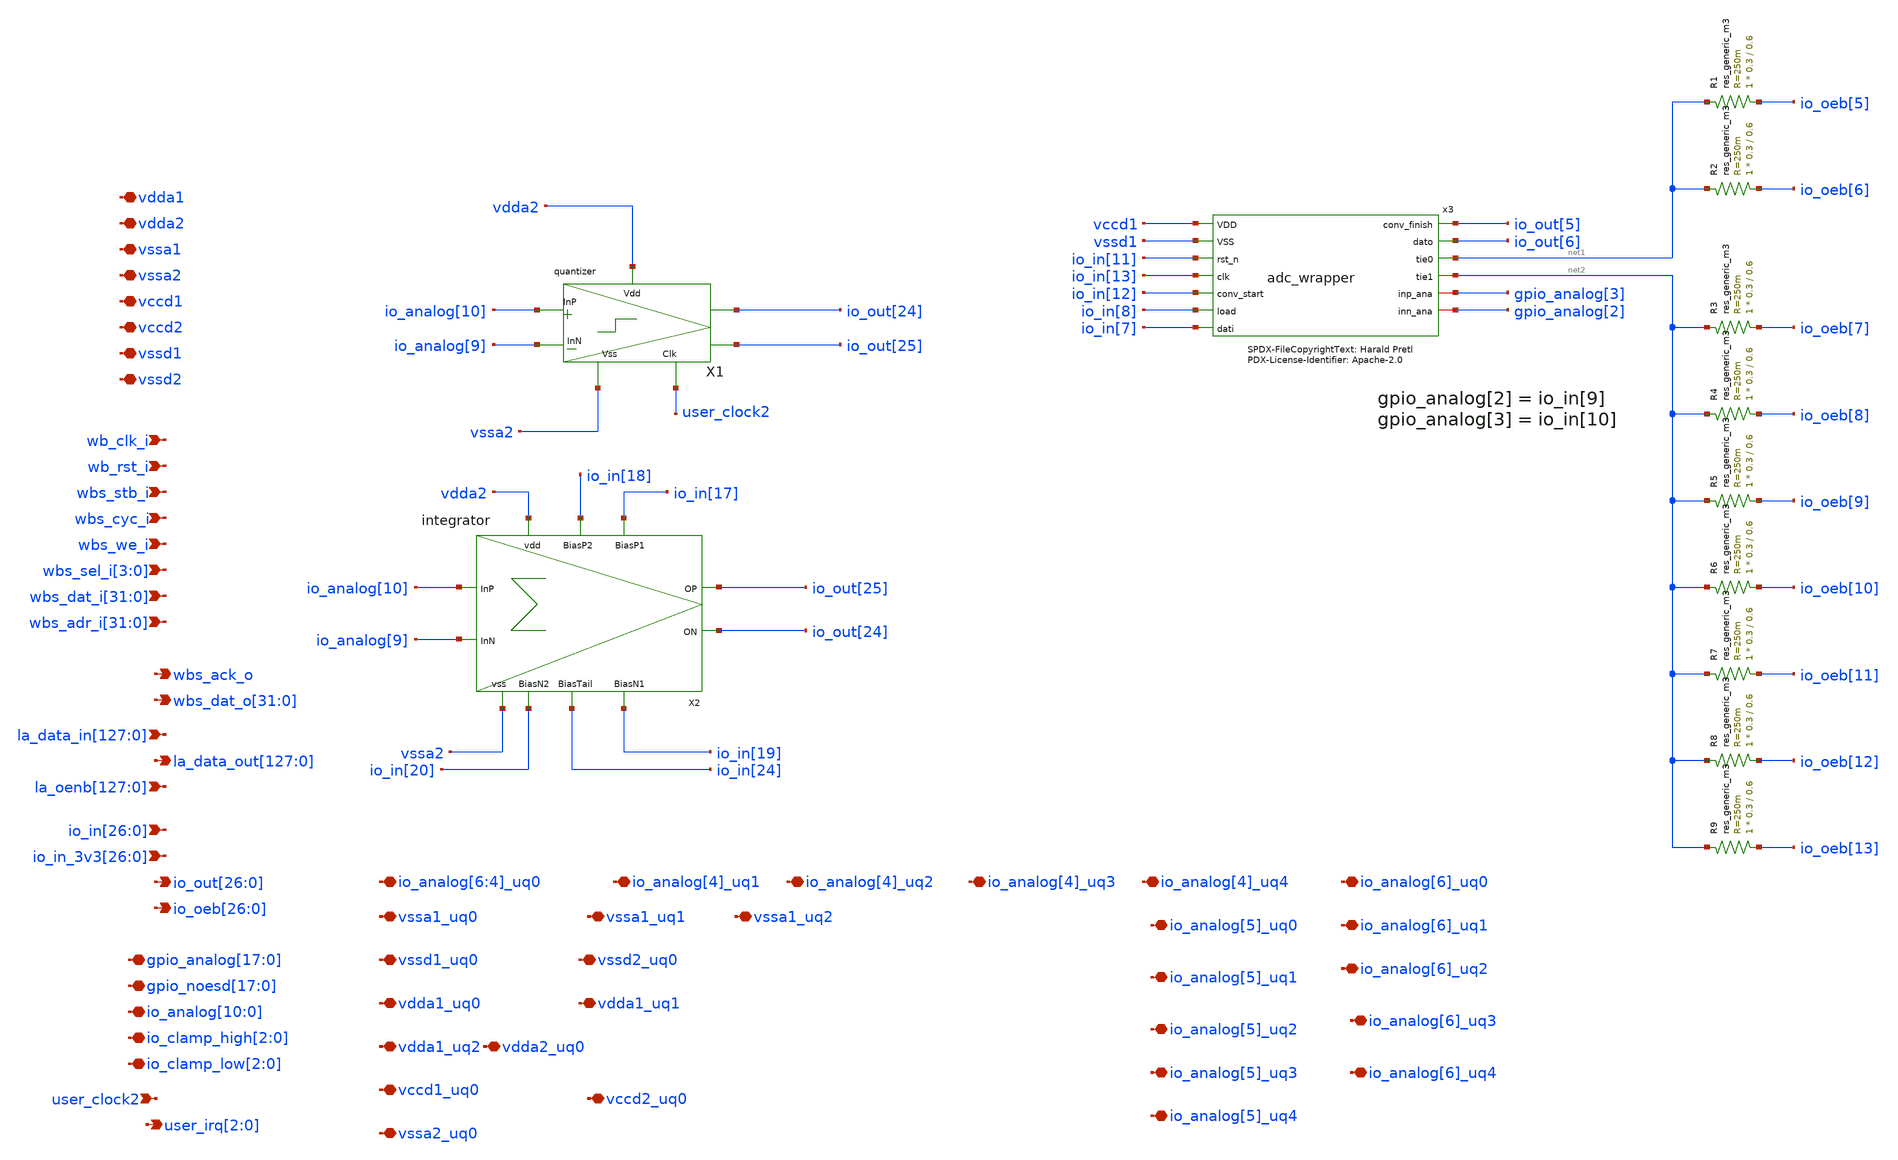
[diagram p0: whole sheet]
** sch_path: xschem/user_analog_project_wrapper_empty.sch
**.subckt user_analog_project_wrapper_empty vdda1 vdda2 vssa1 vssa2 vccd1 vccd2 vssd1 vssd2 wb_clk_i
*+ wb_rst_i wbs_stb_i wbs_cyc_i wbs_we_i wbs_sel_i[3],wbs_sel_i[2],wbs_sel_i[1],wbs_sel_i[0]
*+ wbs_dat_i[31],wbs_dat_i[30],wbs_dat_i[29],wbs_dat_i[28],wbs_dat_i[27],wbs_dat_i[26],wbs_dat_i[25],wbs_dat_i[24],wbs_dat_i[23],wbs_dat_i[22],wbs_dat_i[21],wbs_dat_i[20],wbs_dat_i[19],wbs_dat_i[18],wbs_dat_i[17],wbs_dat_i[16],wbs_dat_i[15],wbs_dat_i[14],wbs_dat_i[13],wbs_dat_i[12],wbs_dat_i[11],wbs_dat_i[10],wbs_dat_i[9],wbs_dat_i[8],wbs_dat_i[7],wbs_dat_i[6],wbs_dat_i[5],wbs_dat_i[4],wbs_dat_i[3],wbs_dat_i[2],wbs_dat_i[1],wbs_dat_i[0]
*+ wbs_adr_i[31],wbs_adr_i[30],wbs_adr_i[29],wbs_adr_i[28],wbs_adr_i[27],wbs_adr_i[26],wbs_adr_i[25],wbs_adr_i[24],wbs_adr_i[23],wbs_adr_i[22],wbs_adr_i[21],wbs_adr_i[20],wbs_adr_i[19],wbs_adr_i[18],wbs_adr_i[17],wbs_adr_i[16],wbs_adr_i[15],wbs_adr_i[14],wbs_adr_i[13],wbs_adr_i[12],wbs_adr_i[11],wbs_adr_i[10],wbs_adr_i[9],wbs_adr_i[8],wbs_adr_i[7],wbs_adr_i[6],wbs_adr_i[5],wbs_adr_i[4],wbs_adr_i[3],wbs_adr_i[2],wbs_adr_i[1],wbs_adr_i[0] wbs_ack_o
*+ wbs_dat_o[31],wbs_dat_o[30],wbs_dat_o[29],wbs_dat_o[28],wbs_dat_o[27],wbs_dat_o[26],wbs_dat_o[25],wbs_dat_o[24],wbs_dat_o[23],wbs_dat_o[22],wbs_dat_o[21],wbs_dat_o[20],wbs_dat_o[19],wbs_dat_o[18],wbs_dat_o[17],wbs_dat_o[16],wbs_dat_o[15],wbs_dat_o[14],wbs_dat_o[13],wbs_dat_o[12],wbs_dat_o[11],wbs_dat_o[10],wbs_dat_o[9],wbs_dat_o[8],wbs_dat_o[7],wbs_dat_o[6],wbs_dat_o[5],wbs_dat_o[4],wbs_dat_o[3],wbs_dat_o[2],wbs_dat_o[1],wbs_dat_o[0]
*+ la_data_in[127],la_data_in[126],la_data_in[125],la_data_in[124],la_data_in[123],la_data_in[122],la_data_in[121],la_data_in[120],la_data_in[119],la_data_in[118],la_data_in[117],la_data_in[116],la_data_in[115],la_data_in[114],la_data_in[113],la_data_in[112],la_data_in[111],la_data_in[110],la_data_in[109],la_data_in[108],la_data_in[107],la_data_in[106],la_data_in[105],la_data_in[104],la_data_in[103],la_data_in[102],la_data_in[101],la_data_in[100],la_data_in[99],la_data_in[98],la_data_in[97],la_data_in[96],la_data_in[95],la_data_in[94],la_data_in[93],la_data_in[92],la_data_in[91],la_data_in[90],la_data_in[89],la_data_in[88],la_data_in[87],la_data_in[86],la_data_in[85],la_data_in[84],la_data_in[83],la_data_in[82],la_data_in[81],la_data_in[80],la_data_in[79],la_data_in[78],la_data_in[77],la_data_in[76],la_data_in[75],la_data_in[74],la_data_in[73],la_data_in[72],la_data_in[71],la_data_in[70],la_data_in[69],la_data_in[68],la_data_in[67],la_data_in[66],la_data_in[65],la_data_in[64],la_data_in[63],la_data_in[62],la_data_in[61],la_data_in[60],la_data_in[59],la_data_in[58],la_data_in[57],la_data_in[56],la_data_in[55],la_data_in[54],la_data_in[53],la_data_in[52],la_data_in[51],la_data_in[50],la_data_in[49],la_data_in[48],la_data_in[47],la_data_in[46],la_data_in[45],la_data_in[44],la_data_in[43],la_data_in[42],la_data_in[41],la_data_in[40],la_data_in[39],la_data_in[38],la_data_in[37],la_data_in[36],la_data_in[35],la_data_in[34],la_data_in[33],la_data_in[32],la_data_in[31],la_data_in[30],la_data_in[29],la_data_in[28],la_data_in[27],la_data_in[26],la_data_in[25],la_data_in[24],la_data_in[23],la_data_in[22],la_data_in[21],la_data_in[20],la_data_in[19],la_data_in[18],la_data_in[17],la_data_in[16],la_data_in[15],la_data_in[14],la_data_in[13],la_data_in[12],la_data_in[11],la_data_in[10],la_data_in[9],la_data_in[8],la_data_in[7],la_data_in[6],la_data_in[5],la_data_in[4],la_data_in[3],la_data_in[2],la_data_in[1],la_data_in[0]
*+ la_data_out[127],la_data_out[126],la_data_out[125],la_data_out[124],la_data_out[123],la_data_out[122],la_data_out[121],la_data_out[120],la_data_out[119],la_data_out[118],la_data_out[117],la_data_out[116],la_data_out[115],la_data_out[114],la_data_out[113],la_data_out[112],la_data_out[111],la_data_out[110],la_data_out[109],la_data_out[108],la_data_out[107],la_data_out[106],la_data_out[105],la_data_out[104],la_data_out[103],la_data_out[102],la_data_out[101],la_data_out[100],la_data_out[99],la_data_out[98],la_data_out[97],la_data_out[96],la_data_out[95],la_data_out[94],la_data_out[93],la_data_out[92],la_data_out[91],la_data_out[90],la_data_out[89],la_data_out[88],la_data_out[87],la_data_out[86],la_data_out[85],la_data_out[84],la_data_out[83],la_data_out[82],la_data_out[81],la_data_out[80],la_data_out[79],la_data_out[78],la_data_out[77],la_data_out[76],la_data_out[75],la_data_out[74],la_data_out[73],la_data_out[72],la_data_out[71],la_data_out[70],la_data_out[69],la_data_out[68],la_data_out[67],la_data_out[66],la_data_out[65],la_data_out[64],la_data_out[63],la_data_out[62],la_data_out[61],la_data_out[60],la_data_out[59],la_data_out[58],la_data_out[57],la_data_out[56],la_data_out[55],la_data_out[54],la_data_out[53],la_data_out[52],la_data_out[51],la_data_out[50],la_data_out[49],la_data_out[48],la_data_out[47],la_data_out[46],la_data_out[45],la_data_out[44],la_data_out[43],la_data_out[42],la_data_out[41],la_data_out[40],la_data_out[39],la_data_out[38],la_data_out[37],la_data_out[36],la_data_out[35],la_data_out[34],la_data_out[33],la_data_out[32],la_data_out[31],la_data_out[30],la_data_out[29],la_data_out[28],la_data_out[27],la_data_out[26],la_data_out[25],la_data_out[24],la_data_out[23],la_data_out[22],la_data_out[21],la_data_out[20],la_data_out[19],la_data_out[18],la_data_out[17],la_data_out[16],la_data_out[15],la_data_out[14],la_data_out[13],la_data_out[12],la_data_out[11],la_data_out[10],la_data_out[9],la_data_out[8],la_data_out[7],la_data_out[6],la_data_out[5],la_data_out[4],la_data_out[3],la_data_out[2],la_data_out[1],la_data_out[0]
*+ io_in[26],io_in[25],io_in[24],io_in[23],io_in[22],io_in[21],io_in[20],io_in[19],io_in[18],io_in[17],io_in[16],io_in[15],io_in[14],io_in[13],io_in[12],io_in[11],io_in[10],io_in[9],io_in[8],io_in[7],io_in[6],io_in[5],io_in[4],io_in[3],io_in[2],io_in[1],io_in[0]
*+ io_in_3v3[26],io_in_3v3[25],io_in_3v3[24],io_in_3v3[23],io_in_3v3[22],io_in_3v3[21],io_in_3v3[20],io_in_3v3[19],io_in_3v3[18],io_in_3v3[17],io_in_3v3[16],io_in_3v3[15],io_in_3v3[14],io_in_3v3[13],io_in_3v3[12],io_in_3v3[11],io_in_3v3[10],io_in_3v3[9],io_in_3v3[8],io_in_3v3[7],io_in_3v3[6],io_in_3v3[5],io_in_3v3[4],io_in_3v3[3],io_in_3v3[2],io_in_3v3[1],io_in_3v3[0] user_clock2
*+ io_out[26],io_out[25],io_out[24],io_out[23],io_out[22],io_out[21],io_out[20],io_out[19],io_out[18],io_out[17],io_out[16],io_out[15],io_out[14],io_out[13],io_out[12],io_out[11],io_out[10],io_out[9],io_out[8],io_out[7],io_out[6],io_out[5],io_out[4],io_out[3],io_out[2],io_out[1],io_out[0]
*+ io_oeb[26],io_oeb[25],io_oeb[24],io_oeb[23],io_oeb[22],io_oeb[21],io_oeb[20],io_oeb[19],io_oeb[18],io_oeb[17],io_oeb[16],io_oeb[15],io_oeb[14],io_oeb[13],io_oeb[12],io_oeb[11],io_oeb[10],io_oeb[9],io_oeb[8],io_oeb[7],io_oeb[6],io_oeb[5],io_oeb[4],io_oeb[3],io_oeb[2],io_oeb[1],io_oeb[0]
*+ gpio_analog[17],gpio_analog[16],gpio_analog[15],gpio_analog[14],gpio_analog[13],gpio_analog[12],gpio_analog[11],gpio_analog[10],gpio_analog[9],gpio_analog[8],gpio_analog[7],gpio_analog[6],gpio_analog[5],gpio_analog[4],gpio_analog[3],gpio_analog[2],gpio_analog[1],gpio_analog[0]
*+ gpio_noesd[17],gpio_noesd[16],gpio_noesd[15],gpio_noesd[14],gpio_noesd[13],gpio_noesd[12],gpio_noesd[11],gpio_noesd[10],gpio_noesd[9],gpio_noesd[8],gpio_noesd[7],gpio_noesd[6],gpio_noesd[5],gpio_noesd[4],gpio_noesd[3],gpio_noesd[2],gpio_noesd[1],gpio_noesd[0]
*+ io_analog[10],io_analog[9],io_analog[8],io_analog[7],io_analog[6],io_analog[5],io_analog[4],io_analog[3],io_analog[2],io_analog[1],io_analog[0] io_clamp_high[2],io_clamp_high[1],io_clamp_high[0] io_clamp_low[2],io_clamp_low[1],io_clamp_low[0]
*+ user_irq[2],user_irq[1],user_irq[0]
*+ la_oenb[127],la_oenb[126],la_oenb[125],la_oenb[124],la_oenb[123],la_oenb[122],la_oenb[121],la_oenb[120],la_oenb[119],la_oenb[118],la_oenb[117],la_oenb[116],la_oenb[115],la_oenb[114],la_oenb[113],la_oenb[112],la_oenb[111],la_oenb[110],la_oenb[109],la_oenb[108],la_oenb[107],la_oenb[106],la_oenb[105],la_oenb[104],la_oenb[103],la_oenb[102],la_oenb[101],la_oenb[100],la_oenb[99],la_oenb[98],la_oenb[97],la_oenb[96],la_oenb[95],la_oenb[94],la_oenb[93],la_oenb[92],la_oenb[91],la_oenb[90],la_oenb[89],la_oenb[88],la_oenb[87],la_oenb[86],la_oenb[85],la_oenb[84],la_oenb[83],la_oenb[82],la_oenb[81],la_oenb[80],la_oenb[79],la_oenb[78],la_oenb[77],la_oenb[76],la_oenb[75],la_oenb[74],la_oenb[73],la_oenb[72],la_oenb[71],la_oenb[70],la_oenb[69],la_oenb[68],la_oenb[67],la_oenb[66],la_oenb[65],la_oenb[64],la_oenb[63],la_oenb[62],la_oenb[61],la_oenb[60],la_oenb[59],la_oenb[58],la_oenb[57],la_oenb[56],la_oenb[55],la_oenb[54],la_oenb[53],la_oenb[52],la_oenb[51],la_oenb[50],la_oenb[49],la_oenb[48],la_oenb[47],la_oenb[46],la_oenb[45],la_oenb[44],la_oenb[43],la_oenb[42],la_oenb[41],la_oenb[40],la_oenb[39],la_oenb[38],la_oenb[37],la_oenb[36],la_oenb[35],la_oenb[34],la_oenb[33],la_oenb[32],la_oenb[31],la_oenb[30],la_oenb[29],la_oenb[28],la_oenb[27],la_oenb[26],la_oenb[25],la_oenb[24],la_oenb[23],la_oenb[22],la_oenb[21],la_oenb[20],la_oenb[19],la_oenb[18],la_oenb[17],la_oenb[16],la_oenb[15],la_oenb[14],la_oenb[13],la_oenb[12],la_oenb[11],la_oenb[10],la_oenb[9],la_oenb[8],la_oenb[7],la_oenb[6],la_oenb[5],la_oenb[4],la_oenb[3],la_oenb[2],la_oenb[1],la_oenb[0] io_analog[6]_uq0,io_analog[5]_uq0,io_analog[4]_uq0 vssa1_uq0 vdda1_uq0 vdda1_uq2 vccd1_uq0
*+ vssa2_uq0 vccd2_uq0 vssa1_uq1 vssa1_uq2 vdda1_uq1 vssd1_uq0 vssd2_uq0 vdda2_uq0 io_analog[4]_uq1
*+ io_analog[4]_uq2 io_analog[4]_uq3 io_analog[4]_uq4 io_analog[5]_uq0 io_analog[5]_uq1 io_analog[5]_uq2
*+ io_analog[5]_uq3 io_analog[5]_uq4 io_analog[6]_uq0 io_analog[6]_uq1 io_analog[6]_uq2 io_analog[6]_uq3
*+ io_analog[6]_uq4
*.iopin vdda1
*.iopin vdda2
*.iopin vssa1
*.iopin vssa2
*.iopin vccd1
*.iopin vccd2
*.iopin vssd1
*.iopin vssd2
*.ipin wb_clk_i
*.ipin wb_rst_i
*.ipin wbs_stb_i
*.ipin wbs_cyc_i
*.ipin wbs_we_i
*.ipin wbs_sel_i[3],wbs_sel_i[2],wbs_sel_i[1],wbs_sel_i[0]
*.ipin
*+ wbs_dat_i[31],wbs_dat_i[30],wbs_dat_i[29],wbs_dat_i[28],wbs_dat_i[27],wbs_dat_i[26],wbs_dat_i[25],wbs_dat_i[24],wbs_dat_i[23],wbs_dat_i[22],wbs_dat_i[21],wbs_dat_i[20],wbs_dat_i[19],wbs_dat_i[18],wbs_dat_i[17],wbs_dat_i[16],wbs_dat_i[15],wbs_dat_i[14],wbs_dat_i[13],wbs_dat_i[12],wbs_dat_i[11],wbs_dat_i[10],wbs_dat_i[9],wbs_dat_i[8],wbs_dat_i[7],wbs_dat_i[6],wbs_dat_i[5],wbs_dat_i[4],wbs_dat_i[3],wbs_dat_i[2],wbs_dat_i[1],wbs_dat_i[0]
*.ipin
*+ wbs_adr_i[31],wbs_adr_i[30],wbs_adr_i[29],wbs_adr_i[28],wbs_adr_i[27],wbs_adr_i[26],wbs_adr_i[25],wbs_adr_i[24],wbs_adr_i[23],wbs_adr_i[22],wbs_adr_i[21],wbs_adr_i[20],wbs_adr_i[19],wbs_adr_i[18],wbs_adr_i[17],wbs_adr_i[16],wbs_adr_i[15],wbs_adr_i[14],wbs_adr_i[13],wbs_adr_i[12],wbs_adr_i[11],wbs_adr_i[10],wbs_adr_i[9],wbs_adr_i[8],wbs_adr_i[7],wbs_adr_i[6],wbs_adr_i[5],wbs_adr_i[4],wbs_adr_i[3],wbs_adr_i[2],wbs_adr_i[1],wbs_adr_i[0]
*.opin wbs_ack_o
*.opin
*+ wbs_dat_o[31],wbs_dat_o[30],wbs_dat_o[29],wbs_dat_o[28],wbs_dat_o[27],wbs_dat_o[26],wbs_dat_o[25],wbs_dat_o[24],wbs_dat_o[23],wbs_dat_o[22],wbs_dat_o[21],wbs_dat_o[20],wbs_dat_o[19],wbs_dat_o[18],wbs_dat_o[17],wbs_dat_o[16],wbs_dat_o[15],wbs_dat_o[14],wbs_dat_o[13],wbs_dat_o[12],wbs_dat_o[11],wbs_dat_o[10],wbs_dat_o[9],wbs_dat_o[8],wbs_dat_o[7],wbs_dat_o[6],wbs_dat_o[5],wbs_dat_o[4],wbs_dat_o[3],wbs_dat_o[2],wbs_dat_o[1],wbs_dat_o[0]
*.ipin
*+ la_data_in[127],la_data_in[126],la_data_in[125],la_data_in[124],la_data_in[123],la_data_in[122],la_data_in[121],la_data_in[120],la_data_in[119],la_data_in[118],la_data_in[117],la_data_in[116],la_data_in[115],la_data_in[114],la_data_in[113],la_data_in[112],la_data_in[111],la_data_in[110],la_data_in[109],la_data_in[108],la_data_in[107],la_data_in[106],la_data_in[105],la_data_in[104],la_data_in[103],la_data_in[102],la_data_in[101],la_data_in[100],la_data_in[99],la_data_in[98],la_data_in[97],la_data_in[96],la_data_in[95],la_data_in[94],la_data_in[93],la_data_in[92],la_data_in[91],la_data_in[90],la_data_in[89],la_data_in[88],la_data_in[87],la_data_in[86],la_data_in[85],la_data_in[84],la_data_in[83],la_data_in[82],la_data_in[81],la_data_in[80],la_data_in[79],la_data_in[78],la_data_in[77],la_data_in[76],la_data_in[75],la_data_in[74],la_data_in[73],la_data_in[72],la_data_in[71],la_data_in[70],la_data_in[69],la_data_in[68],la_data_in[67],la_data_in[66],la_data_in[65],la_data_in[64],la_data_in[63],la_data_in[62],la_data_in[61],la_data_in[60],la_data_in[59],la_data_in[58],la_data_in[57],la_data_in[56],la_data_in[55],la_data_in[54],la_data_in[53],la_data_in[52],la_data_in[51],la_data_in[50],la_data_in[49],la_data_in[48],la_data_in[47],la_data_in[46],la_data_in[45],la_data_in[44],la_data_in[43],la_data_in[42],la_data_in[41],la_data_in[40],la_data_in[39],la_data_in[38],la_data_in[37],la_data_in[36],la_data_in[35],la_data_in[34],la_data_in[33],la_data_in[32],la_data_in[31],la_data_in[30],la_data_in[29],la_data_in[28],la_data_in[27],la_data_in[26],la_data_in[25],la_data_in[24],la_data_in[23],la_data_in[22],la_data_in[21],la_data_in[20],la_data_in[19],la_data_in[18],la_data_in[17],la_data_in[16],la_data_in[15],la_data_in[14],la_data_in[13],la_data_in[12],la_data_in[11],la_data_in[10],la_data_in[9],la_data_in[8],la_data_in[7],la_data_in[6],la_data_in[5],la_data_in[4],la_data_in[3],la_data_in[2],la_data_in[1],la_data_in[0]
*.opin
*+ la_data_out[127],la_data_out[126],la_data_out[125],la_data_out[124],la_data_out[123],la_data_out[122],la_data_out[121],la_data_out[120],la_data_out[119],la_data_out[118],la_data_out[117],la_data_out[116],la_data_out[115],la_data_out[114],la_data_out[113],la_data_out[112],la_data_out[111],la_data_out[110],la_data_out[109],la_data_out[108],la_data_out[107],la_data_out[106],la_data_out[105],la_data_out[104],la_data_out[103],la_data_out[102],la_data_out[101],la_data_out[100],la_data_out[99],la_data_out[98],la_data_out[97],la_data_out[96],la_data_out[95],la_data_out[94],la_data_out[93],la_data_out[92],la_data_out[91],la_data_out[90],la_data_out[89],la_data_out[88],la_data_out[87],la_data_out[86],la_data_out[85],la_data_out[84],la_data_out[83],la_data_out[82],la_data_out[81],la_data_out[80],la_data_out[79],la_data_out[78],la_data_out[77],la_data_out[76],la_data_out[75],la_data_out[74],la_data_out[73],la_data_out[72],la_data_out[71],la_data_out[70],la_data_out[69],la_data_out[68],la_data_out[67],la_data_out[66],la_data_out[65],la_data_out[64],la_data_out[63],la_data_out[62],la_data_out[61],la_data_out[60],la_data_out[59],la_data_out[58],la_data_out[57],la_data_out[56],la_data_out[55],la_data_out[54],la_data_out[53],la_data_out[52],la_data_out[51],la_data_out[50],la_data_out[49],la_data_out[48],la_data_out[47],la_data_out[46],la_data_out[45],la_data_out[44],la_data_out[43],la_data_out[42],la_data_out[41],la_data_out[40],la_data_out[39],la_data_out[38],la_data_out[37],la_data_out[36],la_data_out[35],la_data_out[34],la_data_out[33],la_data_out[32],la_data_out[31],la_data_out[30],la_data_out[29],la_data_out[28],la_data_out[27],la_data_out[26],la_data_out[25],la_data_out[24],la_data_out[23],la_data_out[22],la_data_out[21],la_data_out[20],la_data_out[19],la_data_out[18],la_data_out[17],la_data_out[16],la_data_out[15],la_data_out[14],la_data_out[13],la_data_out[12],la_data_out[11],la_data_out[10],la_data_out[9],la_data_out[8],la_data_out[7],la_data_out[6],la_data_out[5],la_data_out[4],la_data_out[3],la_data_out[2],la_data_out[1],la_data_out[0]
*.ipin
*+ io_in[26],io_in[25],io_in[24],io_in[23],io_in[22],io_in[21],io_in[20],io_in[19],io_in[18],io_in[17],io_in[16],io_in[15],io_in[14],io_in[13],io_in[12],io_in[11],io_in[10],io_in[9],io_in[8],io_in[7],io_in[6],io_in[5],io_in[4],io_in[3],io_in[2],io_in[1],io_in[0]
*.ipin
*+ io_in_3v3[26],io_in_3v3[25],io_in_3v3[24],io_in_3v3[23],io_in_3v3[22],io_in_3v3[21],io_in_3v3[20],io_in_3v3[19],io_in_3v3[18],io_in_3v3[17],io_in_3v3[16],io_in_3v3[15],io_in_3v3[14],io_in_3v3[13],io_in_3v3[12],io_in_3v3[11],io_in_3v3[10],io_in_3v3[9],io_in_3v3[8],io_in_3v3[7],io_in_3v3[6],io_in_3v3[5],io_in_3v3[4],io_in_3v3[3],io_in_3v3[2],io_in_3v3[1],io_in_3v3[0]
*.ipin user_clock2
*.opin
*+ io_out[26],io_out[25],io_out[24],io_out[23],io_out[22],io_out[21],io_out[20],io_out[19],io_out[18],io_out[17],io_out[16],io_out[15],io_out[14],io_out[13],io_out[12],io_out[11],io_out[10],io_out[9],io_out[8],io_out[7],io_out[6],io_out[5],io_out[4],io_out[3],io_out[2],io_out[1],io_out[0]
*.opin
*+ io_oeb[26],io_oeb[25],io_oeb[24],io_oeb[23],io_oeb[22],io_oeb[21],io_oeb[20],io_oeb[19],io_oeb[18],io_oeb[17],io_oeb[16],io_oeb[15],io_oeb[14],io_oeb[13],io_oeb[12],io_oeb[11],io_oeb[10],io_oeb[9],io_oeb[8],io_oeb[7],io_oeb[6],io_oeb[5],io_oeb[4],io_oeb[3],io_oeb[2],io_oeb[1],io_oeb[0]
*.iopin
*+ gpio_analog[17],gpio_analog[16],gpio_analog[15],gpio_analog[14],gpio_analog[13],gpio_analog[12],gpio_analog[11],gpio_analog[10],gpio_analog[9],gpio_analog[8],gpio_analog[7],gpio_analog[6],gpio_analog[5],gpio_analog[4],gpio_analog[3],gpio_analog[2],gpio_analog[1],gpio_analog[0]
*.iopin
*+ gpio_noesd[17],gpio_noesd[16],gpio_noesd[15],gpio_noesd[14],gpio_noesd[13],gpio_noesd[12],gpio_noesd[11],gpio_noesd[10],gpio_noesd[9],gpio_noesd[8],gpio_noesd[7],gpio_noesd[6],gpio_noesd[5],gpio_noesd[4],gpio_noesd[3],gpio_noesd[2],gpio_noesd[1],gpio_noesd[0]
*.iopin
*+ io_analog[10],io_analog[9],io_analog[8],io_analog[7],io_analog[6],io_analog[5],io_analog[4],io_analog[3],io_analog[2],io_analog[1],io_analog[0]
*.iopin io_clamp_high[2],io_clamp_high[1],io_clamp_high[0]
*.iopin io_clamp_low[2],io_clamp_low[1],io_clamp_low[0]
*.opin user_irq[2],user_irq[1],user_irq[0]
*.ipin
*+ la_oenb[127],la_oenb[126],la_oenb[125],la_oenb[124],la_oenb[123],la_oenb[122],la_oenb[121],la_oenb[120],la_oenb[119],la_oenb[118],la_oenb[117],la_oenb[116],la_oenb[115],la_oenb[114],la_oenb[113],la_oenb[112],la_oenb[111],la_oenb[110],la_oenb[109],la_oenb[108],la_oenb[107],la_oenb[106],la_oenb[105],la_oenb[104],la_oenb[103],la_oenb[102],la_oenb[101],la_oenb[100],la_oenb[99],la_oenb[98],la_oenb[97],la_oenb[96],la_oenb[95],la_oenb[94],la_oenb[93],la_oenb[92],la_oenb[91],la_oenb[90],la_oenb[89],la_oenb[88],la_oenb[87],la_oenb[86],la_oenb[85],la_oenb[84],la_oenb[83],la_oenb[82],la_oenb[81],la_oenb[80],la_oenb[79],la_oenb[78],la_oenb[77],la_oenb[76],la_oenb[75],la_oenb[74],la_oenb[73],la_oenb[72],la_oenb[71],la_oenb[70],la_oenb[69],la_oenb[68],la_oenb[67],la_oenb[66],la_oenb[65],la_oenb[64],la_oenb[63],la_oenb[62],la_oenb[61],la_oenb[60],la_oenb[59],la_oenb[58],la_oenb[57],la_oenb[56],la_oenb[55],la_oenb[54],la_oenb[53],la_oenb[52],la_oenb[51],la_oenb[50],la_oenb[49],la_oenb[48],la_oenb[47],la_oenb[46],la_oenb[45],la_oenb[44],la_oenb[43],la_oenb[42],la_oenb[41],la_oenb[40],la_oenb[39],la_oenb[38],la_oenb[37],la_oenb[36],la_oenb[35],la_oenb[34],la_oenb[33],la_oenb[32],la_oenb[31],la_oenb[30],la_oenb[29],la_oenb[28],la_oenb[27],la_oenb[26],la_oenb[25],la_oenb[24],la_oenb[23],la_oenb[22],la_oenb[21],la_oenb[20],la_oenb[19],la_oenb[18],la_oenb[17],la_oenb[16],la_oenb[15],la_oenb[14],la_oenb[13],la_oenb[12],la_oenb[11],la_oenb[10],la_oenb[9],la_oenb[8],la_oenb[7],la_oenb[6],la_oenb[5],la_oenb[4],la_oenb[3],la_oenb[2],la_oenb[1],la_oenb[0]
*.iopin io_analog[6]_uq0,io_analog[5]_uq0,io_analog[4]_uq0
*.iopin vssa1_uq0
*.iopin vdda1_uq0
*.iopin vdda1_uq2
*.iopin vccd1_uq0
*.iopin vssa2_uq0
*.iopin vccd2_uq0
*.iopin vssa1_uq1
*.iopin vssa1_uq2
*.iopin vdda1_uq1
*.iopin vssd1_uq0
*.iopin vssd2_uq0
*.iopin vdda2_uq0
*.iopin io_analog[4]_uq1
*.iopin io_analog[4]_uq2
*.iopin io_analog[4]_uq3
*.iopin io_analog[4]_uq4
*.iopin io_analog[5]_uq0
*.iopin io_analog[5]_uq1
*.iopin io_analog[5]_uq2
*.iopin io_analog[5]_uq3
*.iopin io_analog[5]_uq4
*.iopin io_analog[6]_uq0
*.iopin io_analog[6]_uq1
*.iopin io_analog[6]_uq2
*.iopin io_analog[6]_uq3
*.iopin io_analog[6]_uq4
X1 vssa2 user_clock2 vdda2 io_analog[10] io_analog[9] io_out[24] io_out[25] quantizer
X2 vdda2 io_in[18] io_in[17] io_analog[10] io_analog[9] io_out[25] io_out[24] io_in[19] vssa2
+ io_in[20] io_in[24] integrator
R1 io_oeb[5] net1 sky130_fd_pr__res_generic_m3 W=0.3 L=0.6 m=1
R2 io_oeb[6] net1 sky130_fd_pr__res_generic_m3 W=0.3 L=0.6 m=1
R3 io_oeb[7] net2 sky130_fd_pr__res_generic_m3 W=0.3 L=0.6 m=1
R4 io_oeb[8] net2 sky130_fd_pr__res_generic_m3 W=0.3 L=0.6 m=1
R5 io_oeb[9] net2 sky130_fd_pr__res_generic_m3 W=0.3 L=0.6 m=1
R6 io_oeb[10] net2 sky130_fd_pr__res_generic_m3 W=0.3 L=0.6 m=1
R7 io_oeb[11] net2 sky130_fd_pr__res_generic_m3 W=0.3 L=0.6 m=1
R8 io_oeb[12] net2 sky130_fd_pr__res_generic_m3 W=0.3 L=0.6 m=1
R9 io_oeb[13] net2 sky130_fd_pr__res_generic_m3 W=0.3 L=0.6 m=1
x3 vccd1 vssd1 io_in[11] io_in[13] io_in[12] io_out[5] io_in[8] io_in[7] io_out[6] net1 net2
+ gpio_analog[3] gpio_analog[2] adc_wrapper
**.ends

* expanding   symbol:  caravel_user_project_analog_GTO1/xschem/quantizer.sym # of pins=7
** sym_path: xschem/quantizer.sym
** sch_path: xschem/quantizer.sch
.subckt quantizer Vss Clk vdd InP InN OP ON
*.iopin Vss
*.iopin vdd
*.iopin Clk
*.ipin InP
*.ipin InN
*.iopin ON
*.iopin OP
XM29 nodeA1 InP net1 Vss sky130_fd_pr__nfet_01v8 L=1 W=2 nf=1 ad='int((nf+1)/2) * W/nf * 0.29' as='int((nf+2)/2) * W/nf * 0.29'
+ pd='2*int((nf+1)/2) * (W/nf + 0.29)' ps='2*int((nf+2)/2) * (W/nf + 0.29)' nrd='0.29 / W' nrs='0.29 / W'
+ sa=0 sb=0 sd=0 mult=3 m=3
XM30 NodeA2 InN net1 Vss sky130_fd_pr__nfet_01v8 L=1 W=2 nf=1 ad='int((nf+1)/2) * W/nf * 0.29' as='int((nf+2)/2) * W/nf * 0.29'
+ pd='2*int((nf+1)/2) * (W/nf + 0.29)' ps='2*int((nf+2)/2) * (W/nf + 0.29)' nrd='0.29 / W' nrs='0.29 / W'
+ sa=0 sb=0 sd=0 mult=3 m=3
XM31 OP ON NodeA2 Vss sky130_fd_pr__nfet_01v8 L=1 W=2 nf=1 ad='int((nf+1)/2) * W/nf * 0.29' as='int((nf+2)/2) * W/nf * 0.29'
+ pd='2*int((nf+1)/2) * (W/nf + 0.29)' ps='2*int((nf+2)/2) * (W/nf + 0.29)' nrd='0.29 / W' nrs='0.29 / W'
+ sa=0 sb=0 sd=0 mult=1 m=1
XM32 ON OP nodeA1 Vss sky130_fd_pr__nfet_01v8 L=1 W=2 nf=1 ad='int((nf+1)/2) * W/nf * 0.29' as='int((nf+2)/2) * W/nf * 0.29'
+ pd='2*int((nf+1)/2) * (W/nf + 0.29)' ps='2*int((nf+2)/2) * (W/nf + 0.29)' nrd='0.29 / W' nrs='0.29 / W'
+ sa=0 sb=0 sd=0 mult=1 m=1
XM34 OP ON vdd vdd sky130_fd_pr__pfet_01v8 L=1 W=4 nf=1 ad='int((nf+1)/2) * W/nf * 0.29' as='int((nf+2)/2) * W/nf * 0.29'
+ pd='2*int((nf+1)/2) * (W/nf + 0.29)' ps='2*int((nf+2)/2) * (W/nf + 0.29)' nrd='0.29 / W' nrs='0.29 / W'
+ sa=0 sb=0 sd=0 mult=1 m=1
XM35 ON OP vdd vdd sky130_fd_pr__pfet_01v8 L=1 W=4 nf=1 ad='int((nf+1)/2) * W/nf * 0.29' as='int((nf+2)/2) * W/nf * 0.29'
+ pd='2*int((nf+1)/2) * (W/nf + 0.29)' ps='2*int((nf+2)/2) * (W/nf + 0.29)' nrd='0.29 / W' nrs='0.29 / W'
+ sa=0 sb=0 sd=0 mult=1 m=1
XM36 ON Clk vdd vdd sky130_fd_pr__pfet_01v8 L=1 W=4 nf=1 ad='int((nf+1)/2) * W/nf * 0.29' as='int((nf+2)/2) * W/nf * 0.29'
+ pd='2*int((nf+1)/2) * (W/nf + 0.29)' ps='2*int((nf+2)/2) * (W/nf + 0.29)' nrd='0.29 / W' nrs='0.29 / W'
+ sa=0 sb=0 sd=0 mult=4 m=4
XM37 nodeA1 Clk vdd vdd sky130_fd_pr__pfet_01v8 L=1 W=4 nf=1 ad='int((nf+1)/2) * W/nf * 0.29' as='int((nf+2)/2) * W/nf * 0.29'
+ pd='2*int((nf+1)/2) * (W/nf + 0.29)' ps='2*int((nf+2)/2) * (W/nf + 0.29)' nrd='0.29 / W' nrs='0.29 / W'
+ sa=0 sb=0 sd=0 mult=4 m=4
XM38 OP Clk vdd vdd sky130_fd_pr__pfet_01v8 L=1 W=4 nf=1 ad='int((nf+1)/2) * W/nf * 0.29' as='int((nf+2)/2) * W/nf * 0.29'
+ pd='2*int((nf+1)/2) * (W/nf + 0.29)' ps='2*int((nf+2)/2) * (W/nf + 0.29)' nrd='0.29 / W' nrs='0.29 / W'
+ sa=0 sb=0 sd=0 mult=4 m=4
XM39 NodeA2 Clk vdd vdd sky130_fd_pr__pfet_01v8 L=1 W=4 nf=1 ad='int((nf+1)/2) * W/nf * 0.29' as='int((nf+2)/2) * W/nf * 0.29'
+ pd='2*int((nf+1)/2) * (W/nf + 0.29)' ps='2*int((nf+2)/2) * (W/nf + 0.29)' nrd='0.29 / W' nrs='0.29 / W'
+ sa=0 sb=0 sd=0 mult=4 m=4
XM1 OP Vss Vss Vss sky130_fd_pr__nfet_01v8 L=1 W=2 nf=1 ad='int((nf+1)/2) * W/nf * 0.29' as='int((nf+2)/2) * W/nf * 0.29'
+ pd='2*int((nf+1)/2) * (W/nf + 0.29)' ps='2*int((nf+2)/2) * (W/nf + 0.29)' nrd='0.29 / W' nrs='0.29 / W'
+ sa=0 sb=0 sd=0 mult=5 m=5
XM2 ON Vss Vss Vss sky130_fd_pr__nfet_01v8 L=1 W=2 nf=1 ad='int((nf+1)/2) * W/nf * 0.29' as='int((nf+2)/2) * W/nf * 0.29'
+ pd='2*int((nf+1)/2) * (W/nf + 0.29)' ps='2*int((nf+2)/2) * (W/nf + 0.29)' nrd='0.29 / W' nrs='0.29 / W'
+ sa=0 sb=0 sd=0 mult=5 m=5
XM3 ON vdd vdd vdd sky130_fd_pr__pfet_01v8 L=1 W=4 nf=1 ad='int((nf+1)/2) * W/nf * 0.29' as='int((nf+2)/2) * W/nf * 0.29'
+ pd='2*int((nf+1)/2) * (W/nf + 0.29)' ps='2*int((nf+2)/2) * (W/nf + 0.29)' nrd='0.29 / W' nrs='0.29 / W'
+ sa=0 sb=0 sd=0 mult=1 m=1
XM4 OP vdd vdd vdd sky130_fd_pr__pfet_01v8 L=1 W=4 nf=1 ad='int((nf+1)/2) * W/nf * 0.29' as='int((nf+2)/2) * W/nf * 0.29'
+ pd='2*int((nf+1)/2) * (W/nf + 0.29)' ps='2*int((nf+2)/2) * (W/nf + 0.29)' nrd='0.29 / W' nrs='0.29 / W'
+ sa=0 sb=0 sd=0 mult=1 m=1
XM5 net1 Clk Vss Vss sky130_fd_pr__nfet_01v8 L=1 W=2 nf=1 ad='int((nf+1)/2) * W/nf * 0.29' as='int((nf+2)/2) * W/nf * 0.29'
+ pd='2*int((nf+1)/2) * (W/nf + 0.29)' ps='2*int((nf+2)/2) * (W/nf + 0.29)' nrd='0.29 / W' nrs='0.29 / W'
+ sa=0 sb=0 sd=0 mult=4 m=4
XM6 nodeA1 vdd vdd vdd sky130_fd_pr__pfet_01v8 L=1 W=4 nf=1 ad='int((nf+1)/2) * W/nf * 0.29' as='int((nf+2)/2) * W/nf * 0.29'
+ pd='2*int((nf+1)/2) * (W/nf + 0.29)' ps='2*int((nf+2)/2) * (W/nf + 0.29)' nrd='0.29 / W' nrs='0.29 / W'
+ sa=0 sb=0 sd=0 mult=1 m=1
XM7 NodeA2 vdd vdd vdd sky130_fd_pr__pfet_01v8 L=1 W=4 nf=1 ad='int((nf+1)/2) * W/nf * 0.29' as='int((nf+2)/2) * W/nf * 0.29'
+ pd='2*int((nf+1)/2) * (W/nf + 0.29)' ps='2*int((nf+2)/2) * (W/nf + 0.29)' nrd='0.29 / W' nrs='0.29 / W'
+ sa=0 sb=0 sd=0 mult=1 m=1
.ends


* expanding   symbol:  caravel_user_project_analog_GTO1/xschem/integrator.sym # of pins=11
** sym_path: xschem/integrator.sym
** sch_path: xschem/integrator.sch
.subckt integrator vdd BiasP2 BiasP1 InP InN OP ON BiasN1 vss BiasN2 BiasTail
*.iopin vss
*.iopin BiasN1
*.iopin BiasN2
*.iopin BiasP1
*.iopin BiasP2
*.iopin vdd
*.iopin BiasTail
*.iopin ON
*.iopin OP
*.ipin InP
*.ipin InN
XM15 NodeB InP Tail1 vss sky130_fd_pr__nfet_01v8 L=10 W=20 nf=3 ad='int((nf+1)/2) * W/nf * 0.29' as='int((nf+2)/2) * W/nf * 0.29'
+ pd='2*int((nf+1)/2) * (W/nf + 0.29)' ps='2*int((nf+2)/2) * (W/nf + 0.29)' nrd='0.29 / W' nrs='0.29 / W'
+ sa=0 sb=0 sd=0 mult=1 m=1
XM16 NodeA InN Tail1 vss sky130_fd_pr__nfet_01v8 L=10 W=20 nf=3 ad='int((nf+1)/2) * W/nf * 0.29' as='int((nf+2)/2) * W/nf * 0.29'
+ pd='2*int((nf+1)/2) * (W/nf + 0.29)' ps='2*int((nf+2)/2) * (W/nf + 0.29)' nrd='0.29 / W' nrs='0.29 / W'
+ sa=0 sb=0 sd=0 mult=1 m=1
XM17 Tail1 BiasTail net1 vss sky130_fd_pr__nfet_01v8 L=10 W=20 nf=2 ad='int((nf+1)/2) * W/nf * 0.29'
+ as='int((nf+2)/2) * W/nf * 0.29' pd='2*int((nf+1)/2) * (W/nf + 0.29)' ps='2*int((nf+2)/2) * (W/nf + 0.29)'
+ nrd='0.29 / W' nrs='0.29 / W' sa=0 sb=0 sd=0 mult=2 m=2
XM19 ON BiasP1 NodeA vdd sky130_fd_pr__pfet_01v8 L=10 W=40 nf=2 ad='int((nf+1)/2) * W/nf * 0.29' as='int((nf+2)/2) * W/nf * 0.29'
+ pd='2*int((nf+1)/2) * (W/nf + 0.29)' ps='2*int((nf+2)/2) * (W/nf + 0.29)' nrd='0.29 / W' nrs='0.29 / W'
+ sa=0 sb=0 sd=0 mult=1 m=1
XM20 OP BiasP1 NodeB vdd sky130_fd_pr__pfet_01v8 L=10 W=40 nf=2 ad='int((nf+1)/2) * W/nf * 0.29' as='int((nf+2)/2) * W/nf * 0.29'
+ pd='2*int((nf+1)/2) * (W/nf + 0.29)' ps='2*int((nf+2)/2) * (W/nf + 0.29)' nrd='0.29 / W' nrs='0.29 / W'
+ sa=0 sb=0 sd=0 mult=1 m=1
XM21 NodeB BiasP2 vdd vdd sky130_fd_pr__pfet_01v8 L=10 W=40 nf=5 ad='int((nf+1)/2) * W/nf * 0.29' as='int((nf+2)/2) * W/nf * 0.29'
+ pd='2*int((nf+1)/2) * (W/nf + 0.29)' ps='2*int((nf+2)/2) * (W/nf + 0.29)' nrd='0.29 / W' nrs='0.29 / W'
+ sa=0 sb=0 sd=0 mult=1 m=1
XM22 NodeA BiasP2 vdd vdd sky130_fd_pr__pfet_01v8 L=10 W=40 nf=5 ad='int((nf+1)/2) * W/nf * 0.29' as='int((nf+2)/2) * W/nf * 0.29'
+ pd='2*int((nf+1)/2) * (W/nf + 0.29)' ps='2*int((nf+2)/2) * (W/nf + 0.29)' nrd='0.29 / W' nrs='0.29 / W'
+ sa=0 sb=0 sd=0 mult=1 m=1
XM23 OP BiasN2 net3 vss sky130_fd_pr__nfet_01v8 L=10 W=20 nf=1 ad='int((nf+1)/2) * W/nf * 0.29' as='int((nf+2)/2) * W/nf * 0.29'
+ pd='2*int((nf+1)/2) * (W/nf + 0.29)' ps='2*int((nf+2)/2) * (W/nf + 0.29)' nrd='0.29 / W' nrs='0.29 / W'
+ sa=0 sb=0 sd=0 mult=1 m=1
XM24 ON BiasN2 net2 vss sky130_fd_pr__nfet_01v8 L=10 W=20 nf=1 ad='int((nf+1)/2) * W/nf * 0.29' as='int((nf+2)/2) * W/nf * 0.29'
+ pd='2*int((nf+1)/2) * (W/nf + 0.29)' ps='2*int((nf+2)/2) * (W/nf + 0.29)' nrd='0.29 / W' nrs='0.29 / W'
+ sa=0 sb=0 sd=0 mult=1 m=1
XM25 net2 BiasN1 vss vss sky130_fd_pr__nfet_01v8 L=10 W=20 nf=4 ad='int((nf+1)/2) * W/nf * 0.29' as='int((nf+2)/2) * W/nf * 0.29'
+ pd='2*int((nf+1)/2) * (W/nf + 0.29)' ps='2*int((nf+2)/2) * (W/nf + 0.29)' nrd='0.29 / W' nrs='0.29 / W'
+ sa=0 sb=0 sd=0 mult=1 m=1
XM26 net3 BiasN1 vss vss sky130_fd_pr__nfet_01v8 L=10 W=20 nf=4 ad='int((nf+1)/2) * W/nf * 0.29' as='int((nf+2)/2) * W/nf * 0.29'
+ pd='2*int((nf+1)/2) * (W/nf + 0.29)' ps='2*int((nf+2)/2) * (W/nf + 0.29)' nrd='0.29 / W' nrs='0.29 / W'
+ sa=0 sb=0 sd=0 mult=1 m=1
C1 ON OP 0.8p m=1
C2 OP ON 0.8p m=1
XM54 net1 OP vss vss sky130_fd_pr__nfet_01v8 L=10 W=20 nf=1 ad='int((nf+1)/2) * W/nf * 0.29' as='int((nf+2)/2) * W/nf * 0.29'
+ pd='2*int((nf+1)/2) * (W/nf + 0.29)' ps='2*int((nf+2)/2) * (W/nf + 0.29)' nrd='0.29 / W' nrs='0.29 / W'
+ sa=0 sb=0 sd=0 mult=1 m=1
XM58 net1 ON vss vss sky130_fd_pr__nfet_01v8 L=10 W=20 nf=1 ad='int((nf+1)/2) * W/nf * 0.29' as='int((nf+2)/2) * W/nf * 0.29'
+ pd='2*int((nf+1)/2) * (W/nf + 0.29)' ps='2*int((nf+2)/2) * (W/nf + 0.29)' nrd='0.29 / W' nrs='0.29 / W'
+ sa=0 sb=0 sd=0 mult=1 m=1
XM1 vss vss vss vss sky130_fd_pr__nfet_01v8 L=10 W=20 nf=1 ad='int((nf+1)/2) * W/nf * 0.29' as='int((nf+2)/2) * W/nf * 0.29'
+ pd='2*int((nf+1)/2) * (W/nf + 0.29)' ps='2*int((nf+2)/2) * (W/nf + 0.29)' nrd='0.29 / W' nrs='0.29 / W'
+ sa=0 sb=0 sd=0 mult=1 m=1
XM2 NodeB vdd vdd vdd sky130_fd_pr__pfet_01v8 L=10 W=40 nf=1 ad='int((nf+1)/2) * W/nf * 0.29' as='int((nf+2)/2) * W/nf * 0.29'
+ pd='2*int((nf+1)/2) * (W/nf + 0.29)' ps='2*int((nf+2)/2) * (W/nf + 0.29)' nrd='0.29 / W' nrs='0.29 / W'
+ sa=0 sb=0 sd=0 mult=1 m=1
XM3 NodeA vdd vdd vdd sky130_fd_pr__pfet_01v8 L=10 W=40 nf=1 ad='int((nf+1)/2) * W/nf * 0.29' as='int((nf+2)/2) * W/nf * 0.29'
+ pd='2*int((nf+1)/2) * (W/nf + 0.29)' ps='2*int((nf+2)/2) * (W/nf + 0.29)' nrd='0.29 / W' nrs='0.29 / W'
+ sa=0 sb=0 sd=0 mult=1 m=1
XM4 net3 vss vss vss sky130_fd_pr__nfet_01v8 L=10 W=20 nf=1 ad='int((nf+1)/2) * W/nf * 0.29' as='int((nf+2)/2) * W/nf * 0.29'
+ pd='2*int((nf+1)/2) * (W/nf + 0.29)' ps='2*int((nf+2)/2) * (W/nf + 0.29)' nrd='0.29 / W' nrs='0.29 / W'
+ sa=0 sb=0 sd=0 mult=1 m=1
XM5 Tail1 vss vss vss sky130_fd_pr__nfet_01v8 L=10 W=20 nf=1 ad='int((nf+1)/2) * W/nf * 0.29' as='int((nf+2)/2) * W/nf * 0.29'
+ pd='2*int((nf+1)/2) * (W/nf + 0.29)' ps='2*int((nf+2)/2) * (W/nf + 0.29)' nrd='0.29 / W' nrs='0.29 / W'
+ sa=0 sb=0 sd=0 mult=1 m=1
XM6 Tail1 vss vss vss sky130_fd_pr__nfet_01v8 L=10 W=20 nf=1 ad='int((nf+1)/2) * W/nf * 0.29' as='int((nf+2)/2) * W/nf * 0.29'
+ pd='2*int((nf+1)/2) * (W/nf + 0.29)' ps='2*int((nf+2)/2) * (W/nf + 0.29)' nrd='0.29 / W' nrs='0.29 / W'
+ sa=0 sb=0 sd=0 mult=1 m=1
XM7 net1 vss vss vss sky130_fd_pr__nfet_01v8 L=10 W=20 nf=1 ad='int((nf+1)/2) * W/nf * 0.29' as='int((nf+2)/2) * W/nf * 0.29'
+ pd='2*int((nf+1)/2) * (W/nf + 0.29)' ps='2*int((nf+2)/2) * (W/nf + 0.29)' nrd='0.29 / W' nrs='0.29 / W'
+ sa=0 sb=0 sd=0 mult=1 m=1
XM8 net1 vss vss vss sky130_fd_pr__nfet_01v8 L=10 W=20 nf=1 ad='int((nf+1)/2) * W/nf * 0.29' as='int((nf+2)/2) * W/nf * 0.29'
+ pd='2*int((nf+1)/2) * (W/nf + 0.29)' ps='2*int((nf+2)/2) * (W/nf + 0.29)' nrd='0.29 / W' nrs='0.29 / W'
+ sa=0 sb=0 sd=0 mult=1 m=1
XM9 NodeA vss vss vss sky130_fd_pr__nfet_01v8 L=10 W=20 nf=1 ad='int((nf+1)/2) * W/nf * 0.29' as='int((nf+2)/2) * W/nf * 0.29'
+ pd='2*int((nf+1)/2) * (W/nf + 0.29)' ps='2*int((nf+2)/2) * (W/nf + 0.29)' nrd='0.29 / W' nrs='0.29 / W'
+ sa=0 sb=0 sd=0 mult=1 m=1
XM10 NodeB vss vss vss sky130_fd_pr__nfet_01v8 L=10 W=20 nf=1 ad='int((nf+1)/2) * W/nf * 0.29' as='int((nf+2)/2) * W/nf * 0.29'
+ pd='2*int((nf+1)/2) * (W/nf + 0.29)' ps='2*int((nf+2)/2) * (W/nf + 0.29)' nrd='0.29 / W' nrs='0.29 / W'
+ sa=0 sb=0 sd=0 mult=1 m=1
XM11 ON vss vss vss sky130_fd_pr__nfet_01v8 L=10 W=20 nf=1 ad='int((nf+1)/2) * W/nf * 0.29' as='int((nf+2)/2) * W/nf * 0.29'
+ pd='2*int((nf+1)/2) * (W/nf + 0.29)' ps='2*int((nf+2)/2) * (W/nf + 0.29)' nrd='0.29 / W' nrs='0.29 / W'
+ sa=0 sb=0 sd=0 mult=1 m=1
XM12 OP vss vss vss sky130_fd_pr__nfet_01v8 L=10 W=20 nf=1 ad='int((nf+1)/2) * W/nf * 0.29' as='int((nf+2)/2) * W/nf * 0.29'
+ pd='2*int((nf+1)/2) * (W/nf + 0.29)' ps='2*int((nf+2)/2) * (W/nf + 0.29)' nrd='0.29 / W' nrs='0.29 / W'
+ sa=0 sb=0 sd=0 mult=1 m=1
.ends

.end
